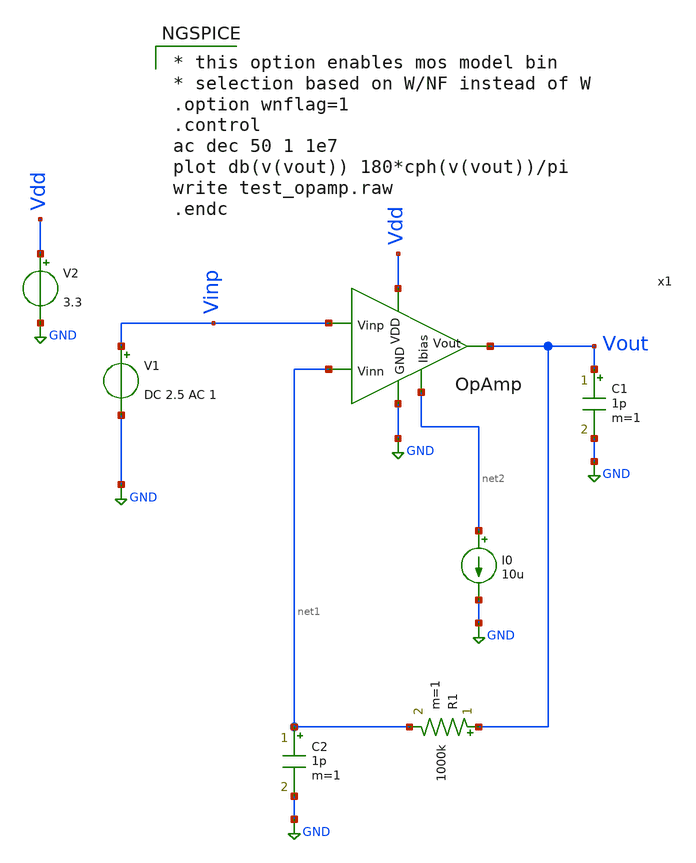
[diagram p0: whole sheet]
** sch_path: xschem/OpAmp_v0/oa_qopenloop_tb.sch
**.subckt oa_qopenloop_tb
V2 Vdd GND 3.3
I0 net2 GND 10u
x1 Vdd Vout net2 net1 Vinp GND OpAmp
C1 Vout GND 1p m=1
R1 Vout net1 1000k m=1
C2 net1 GND 1p m=1
V1 Vinp GND DC 2.5 AC 1
**** begin user architecture code

* this option enables mos model bin
* selection based on W/NF instead of W
.option wnflag=1
.control
ac dec 50 1 1e7
plot db(v(vout)) 180*cph(v(vout))/pi
write test_opamp.raw
.endc


.lib /foss/designs/PDK/sky130B/libs.tech/ngspice/sky130.lib.spice tt
.include /foss/designs/PDK/sky130B/libs.ref/sky130_fd_sc_hvl/spice/sky130_fd_sc_hvl.spice

**** end user architecture code
**.ends
.GLOBAL GND
.end
